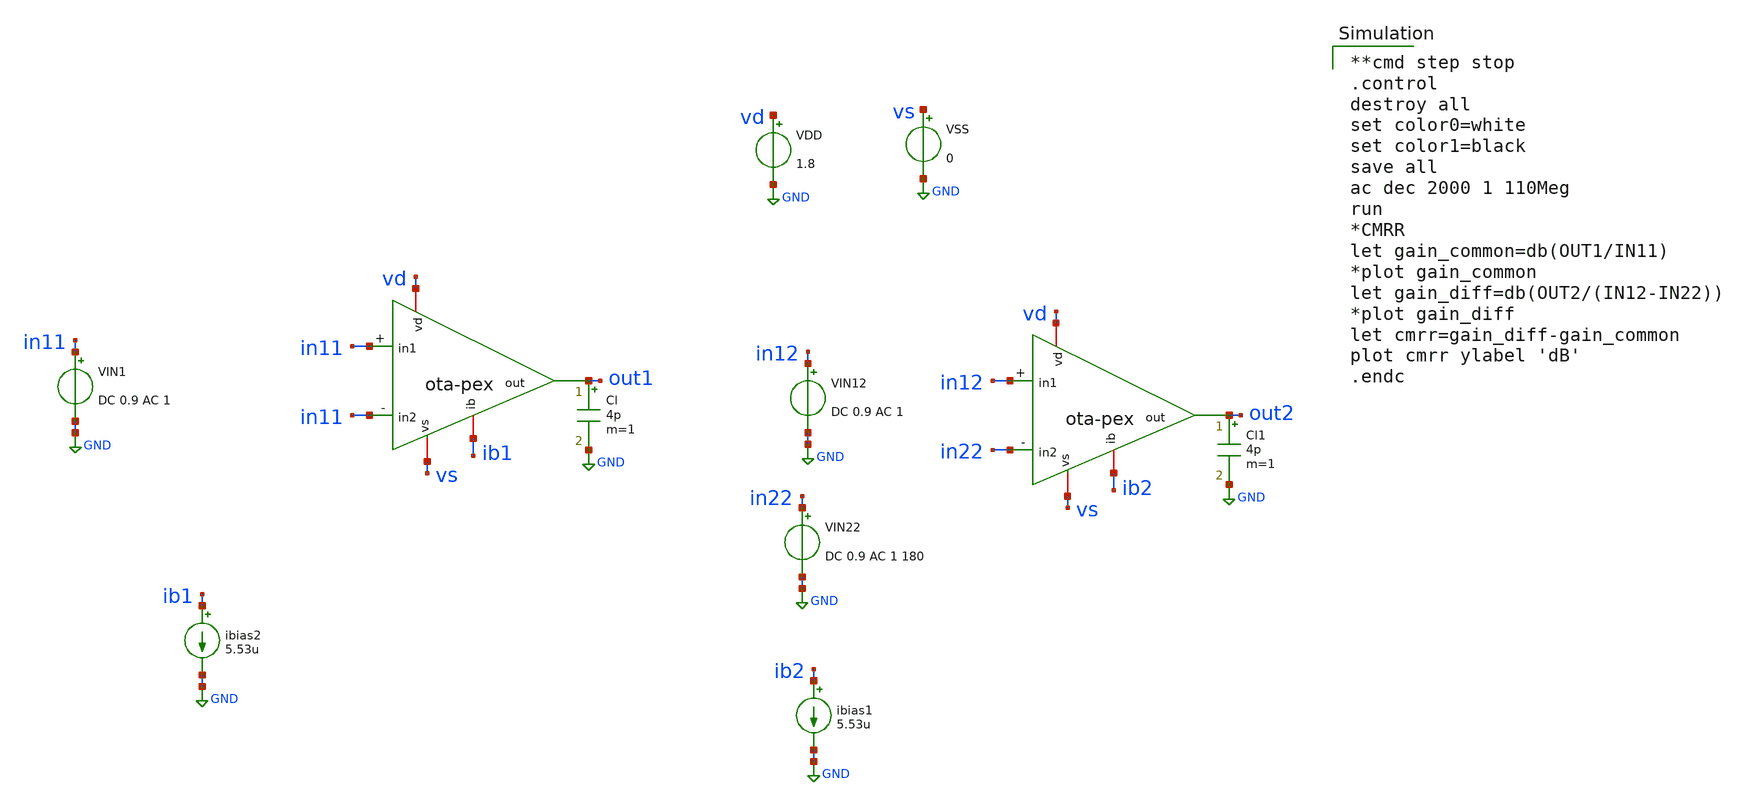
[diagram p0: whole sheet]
** sch_path: ota/xschem/ota_tb-CMRR.sch
* Copyright 2020 Stefan Frederik Schippers
* Licensed under the Apache License, Version 2.0 (the "License");
* you may not use this file except in compliance with the License.
* You may obtain a copy of the License at
* https://www.apache.org/licenses/LICENSE-2.0
* Unless required by applicable law or agreed to in writing, software
* distributed under the License is distributed on an "AS IS" BASIS,
* WITHOUT WARRANTIES OR CONDITIONS OF ANY KIND, either express or implied.
* See the License for the specific language governing permissions and
* limitations under the License.
**.subckt ota_tb-CMRR
ibias2 ib1 GND 5.53u
VDD vd GND 1.8
VSS vs GND 0
VIN12 in12 GND DC 0.9 AC 1
ibias1 ib2 GND 5.53u
VIN22 in22 GND DC 0.9 AC 1 180
Cl out1 GND 4p m=1
Cl1 out2 GND 4p m=1
VIN1 in11 GND DC 0.9 AC 1
X1 vd ib1 out1 in11 in11 vs ota-pex
X2 vd ib2 out2 in22 in12 vs ota-pex
**** begin user architecture code

**cmd step stop
.control
destroy all
set color0=white
set color1=black
save all
ac dec 2000 1 110Meg
run
*CMRR
let gain_common=db(OUT1/IN11)
*plot gain_common
let gain_diff=db(OUT2/(IN12-IN22))
*plot gain_diff
let cmrr=gain_diff-gain_common
plot cmrr ylabel 'dB'
.endc

 .lib $::SKYWATER_MODELS/sky130.lib.spice tt
.include $::SKYWATER_STDCELLS/sky130_fd_sc_hd.spice

**** end user architecture code
**.ends
.GLOBAL GND
.end
